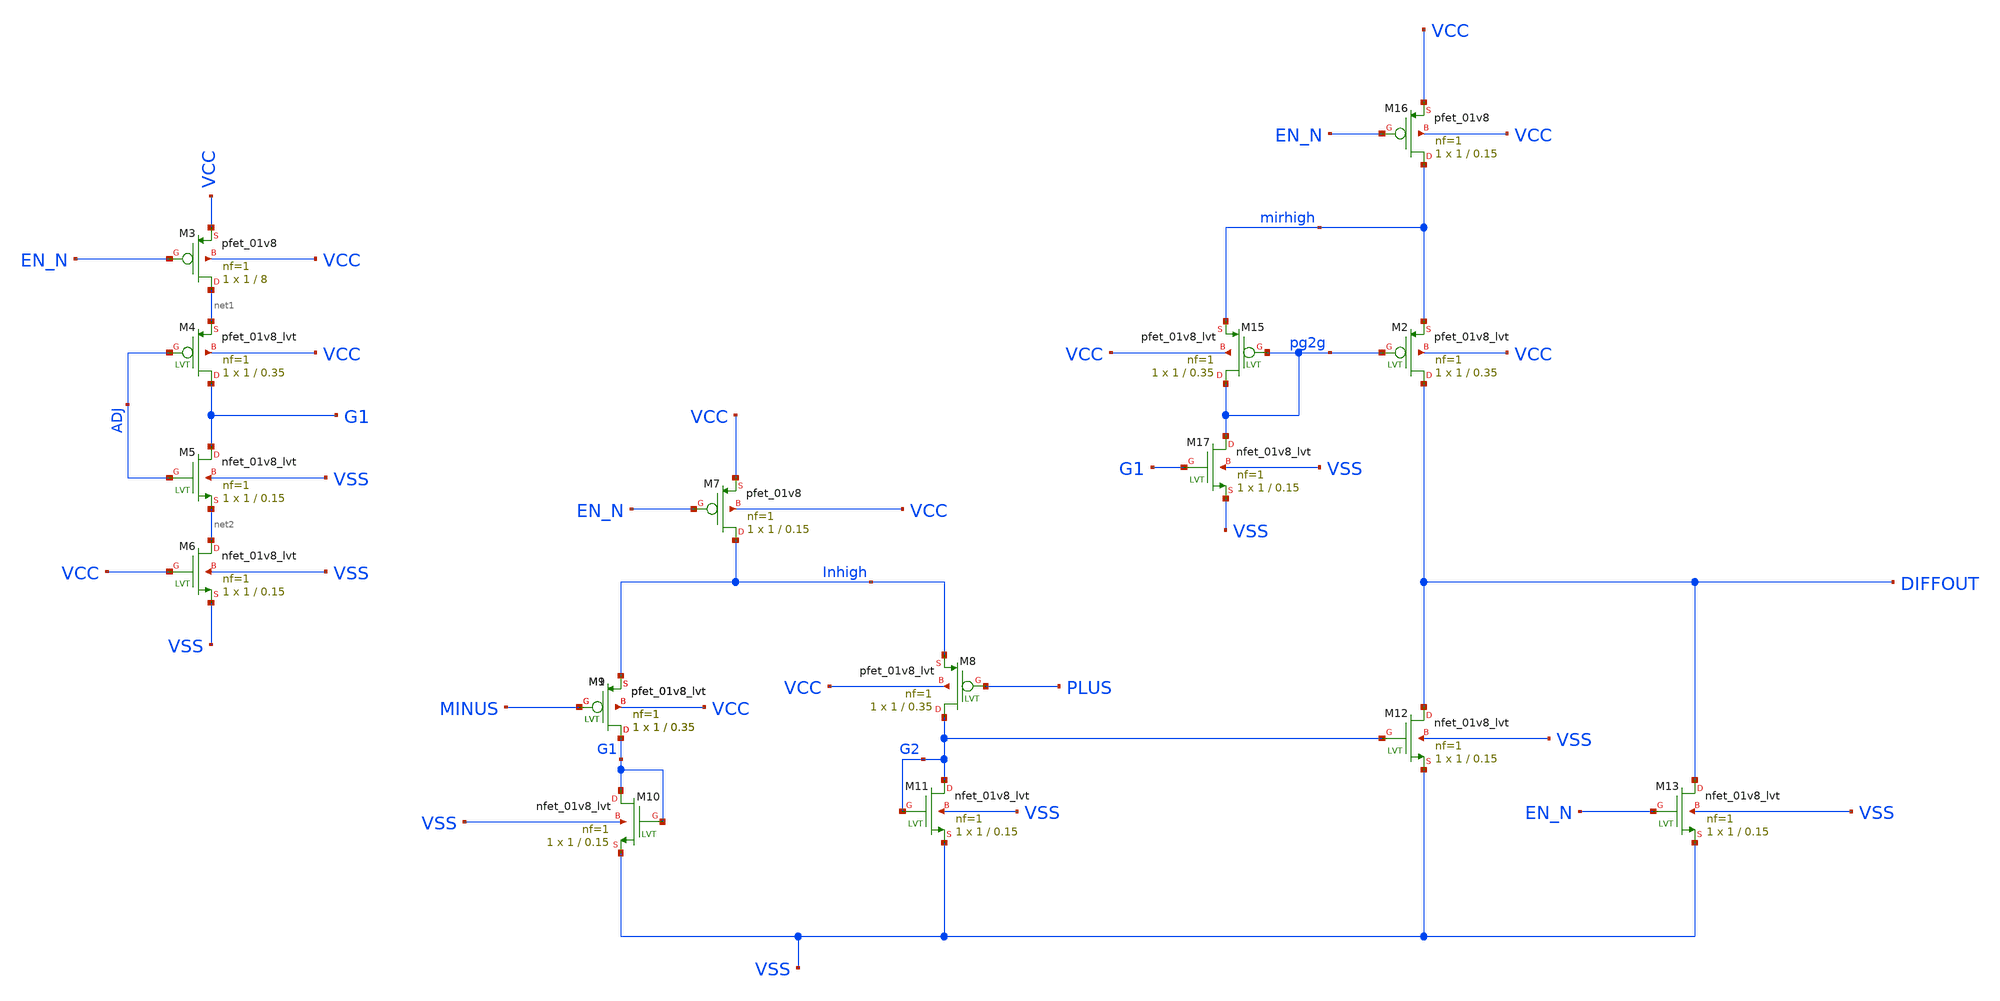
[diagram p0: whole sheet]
** sch_path: comparator.sch
* Copyright 2021 Stefan Frederik Schippers
* Licensed under the Apache License, Version 2.0 (the "License");
* you may not use this file except in compliance with the License.
* You may obtain a copy of the License at
* https://www.apache.org/licenses/LICENSE-2.0
* Unless required by applicable law or agreed to in writing, software
* distributed under the License is distributed on an "AS IS" BASIS,
* WITHOUT WARRANTIES OR CONDITIONS OF ANY KIND, either express or implied.
* See the License for the specific language governing permissions and
* limitations under the License.
**.subckt comparator
XM3 net1 EN_N VCC VCC sky130_fd_pr__pfet_01v8 L=8 W=1 nf=1 ad='int((nf+1)/2) * W/nf * 0.29' as='int((nf+2)/2) * W/nf * 0.29'
+ pd='2*int((nf+1)/2) * (W/nf + 0.29)' ps='2*int((nf+2)/2) * (W/nf + 0.29)' nrd='0.29 / W' nrs='0.29 / W'
+ sa=0 sb=0 sd=0 mult=1 m=1
XM7 Inhigh EN_N VCC VCC sky130_fd_pr__pfet_01v8 L=0.15 W=1 nf=1 ad='int((nf+1)/2) * W/nf * 0.29' as='int((nf+2)/2) * W/nf * 0.29'
+ pd='2*int((nf+1)/2) * (W/nf + 0.29)' ps='2*int((nf+2)/2) * (W/nf + 0.29)' nrd='0.29 / W' nrs='0.29 / W'
+ sa=0 sb=0 sd=0 mult=1 m=1
XM16 mirhigh EN_N VCC VCC sky130_fd_pr__pfet_01v8 L=0.15 W=1 nf=1 ad='int((nf+1)/2) * W/nf * 0.29' as='int((nf+2)/2) * W/nf * 0.29'
+ pd='2*int((nf+1)/2) * (W/nf + 0.29)' ps='2*int((nf+2)/2) * (W/nf + 0.29)' nrd='0.29 / W' nrs='0.29 / W'
+ sa=0 sb=0 sd=0 mult=1 m=1
XM4 G1 ADJ net1 VCC sky130_fd_pr__pfet_01v8_lvt L=0.35 W=1 nf=1 ad='int((nf+1)/2) * W/nf * 0.29' as='int((nf+2)/2) * W/nf * 0.29'
+ pd='2*int((nf+1)/2) * (W/nf + 0.29)' ps='2*int((nf+2)/2) * (W/nf + 0.29)' nrd='0.29 / W' nrs='0.29 / W'
+ sa=0 sb=0 sd=0 mult=1 m=1
XM5 G1 ADJ net2 VSS sky130_fd_pr__nfet_01v8_lvt L=0.15 W=1 nf=1 ad='int((nf+1)/2) * W/nf * 0.29' as='int((nf+2)/2) * W/nf * 0.29'
+ pd='2*int((nf+1)/2) * (W/nf + 0.29)' ps='2*int((nf+2)/2) * (W/nf + 0.29)' nrd='0.29 / W' nrs='0.29 / W'
+ sa=0 sb=0 sd=0 mult=1 m=1
XM6 net2 VCC VSS VSS sky130_fd_pr__nfet_01v8_lvt L=0.15 W=1 nf=1 ad='int((nf+1)/2) * W/nf * 0.29' as='int((nf+2)/2) * W/nf * 0.29'
+ pd='2*int((nf+1)/2) * (W/nf + 0.29)' ps='2*int((nf+2)/2) * (W/nf + 0.29)' nrd='0.29 / W' nrs='0.29 / W'
+ sa=0 sb=0 sd=0 mult=1 m=1
XM9 G1 MINUS Inhigh VCC sky130_fd_pr__pfet_01v8_lvt L=0.35 W=1 nf=1 ad='int((nf+1)/2) * W/nf * 0.29'
+ as='int((nf+2)/2) * W/nf * 0.29' pd='2*int((nf+1)/2) * (W/nf + 0.29)' ps='2*int((nf+2)/2) * (W/nf + 0.29)'
+ nrd='0.29 / W' nrs='0.29 / W' sa=0 sb=0 sd=0 mult=1 m=1
XM8 G2 PLUS Inhigh VCC sky130_fd_pr__pfet_01v8_lvt L=0.35 W=1 nf=1 ad='int((nf+1)/2) * W/nf * 0.29' as='int((nf+2)/2) * W/nf * 0.29'
+ pd='2*int((nf+1)/2) * (W/nf + 0.29)' ps='2*int((nf+2)/2) * (W/nf + 0.29)' nrd='0.29 / W' nrs='0.29 / W'
+ sa=0 sb=0 sd=0 mult=1 m=1
XM11 G2 G2 VSS VSS sky130_fd_pr__nfet_01v8_lvt L=0.15 W=1 nf=1 ad='int((nf+1)/2) * W/nf * 0.29' as='int((nf+2)/2) * W/nf * 0.29'
+ pd='2*int((nf+1)/2) * (W/nf + 0.29)' ps='2*int((nf+2)/2) * (W/nf + 0.29)' nrd='0.29 / W' nrs='0.29 / W'
+ sa=0 sb=0 sd=0 mult=1 m=1
XM10 G1 G1 VSS VSS sky130_fd_pr__nfet_01v8_lvt L=0.15 W=1 nf=1 ad='int((nf+1)/2) * W/nf * 0.29' as='int((nf+2)/2) * W/nf * 0.29'
+ pd='2*int((nf+1)/2) * (W/nf + 0.29)' ps='2*int((nf+2)/2) * (W/nf + 0.29)' nrd='0.29 / W' nrs='0.29 / W'
+ sa=0 sb=0 sd=0 mult=1 m=1
XM12 DIFFOUT G2 VSS VSS sky130_fd_pr__nfet_01v8_lvt L=0.15 W=1 nf=1 ad='int((nf+1)/2) * W/nf * 0.29'
+ as='int((nf+2)/2) * W/nf * 0.29' pd='2*int((nf+1)/2) * (W/nf + 0.29)' ps='2*int((nf+2)/2) * (W/nf + 0.29)'
+ nrd='0.29 / W' nrs='0.29 / W' sa=0 sb=0 sd=0 mult=1 m=1
XM13 DIFFOUT EN_N VSS VSS sky130_fd_pr__nfet_01v8_lvt L=0.15 W=1 nf=1 ad='int((nf+1)/2) * W/nf * 0.29'
+ as='int((nf+2)/2) * W/nf * 0.29' pd='2*int((nf+1)/2) * (W/nf + 0.29)' ps='2*int((nf+2)/2) * (W/nf + 0.29)'
+ nrd='0.29 / W' nrs='0.29 / W' sa=0 sb=0 sd=0 mult=1 m=1
XM17 pg2g G1 VSS VSS sky130_fd_pr__nfet_01v8_lvt L=0.15 W=1 nf=1 ad='int((nf+1)/2) * W/nf * 0.29' as='int((nf+2)/2) * W/nf * 0.29'
+ pd='2*int((nf+1)/2) * (W/nf + 0.29)' ps='2*int((nf+2)/2) * (W/nf + 0.29)' nrd='0.29 / W' nrs='0.29 / W'
+ sa=0 sb=0 sd=0 mult=1 m=1
XM15 pg2g pg2g mirhigh VCC sky130_fd_pr__pfet_01v8_lvt L=0.35 W=1 nf=1 ad='int((nf+1)/2) * W/nf * 0.29'
+ as='int((nf+2)/2) * W/nf * 0.29' pd='2*int((nf+1)/2) * (W/nf + 0.29)' ps='2*int((nf+2)/2) * (W/nf + 0.29)'
+ nrd='0.29 / W' nrs='0.29 / W' sa=0 sb=0 sd=0 mult=1 m=1
XM1 G1 MINUS Inhigh VCC sky130_fd_pr__pfet_01v8_lvt L=0.35 W=1 nf=1 ad='int((nf+1)/2) * W/nf * 0.29'
+ as='int((nf+2)/2) * W/nf * 0.29' pd='2*int((nf+1)/2) * (W/nf + 0.29)' ps='2*int((nf+2)/2) * (W/nf + 0.29)'
+ nrd='0.29 / W' nrs='0.29 / W' sa=0 sb=0 sd=0 mult=1 m=1
XM2 DIFFOUT pg2g mirhigh VCC sky130_fd_pr__pfet_01v8_lvt L=0.35 W=1 nf=1 ad='int((nf+1)/2) * W/nf * 0.29'
+ as='int((nf+2)/2) * W/nf * 0.29' pd='2*int((nf+1)/2) * (W/nf + 0.29)' ps='2*int((nf+2)/2) * (W/nf + 0.29)'
+ nrd='0.29 / W' nrs='0.29 / W' sa=0 sb=0 sd=0 mult=1 m=1
**.ends
.end
